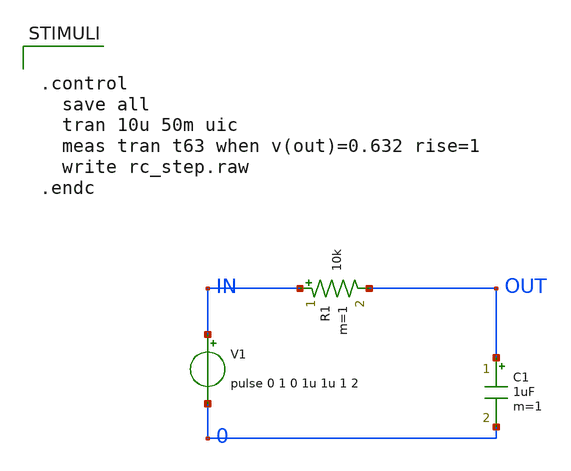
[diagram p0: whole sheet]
** sch_path: doc/mcp/rc_step.sch
**.subckt rc_step
V1 IN 0 pulse 0 1 0 1u 1u 1 2
R1 IN OUT 10k m=1
C1 OUT 0 1uF m=1
**** begin user architecture code


.control
  save all
  tran 10u 50m uic
  meas tran t63 when v(out)=0.632 rise=1
  write rc_step.raw
.endc


**** end user architecture code
**.ends
.end
